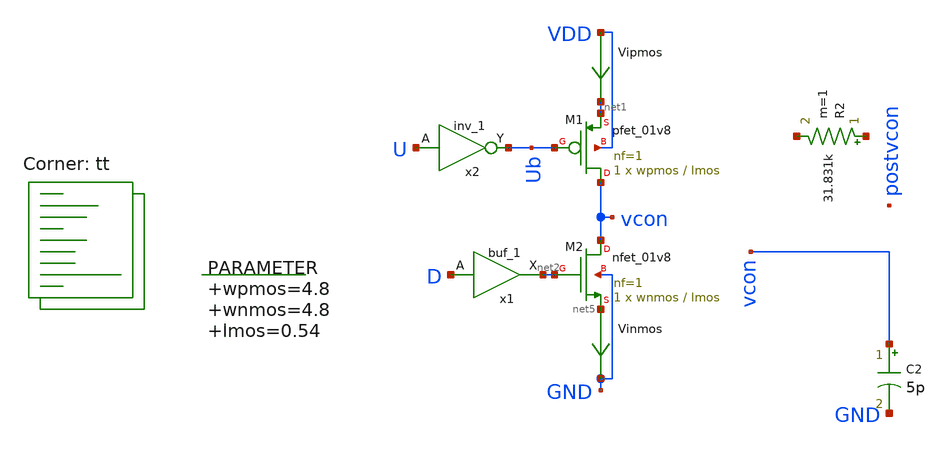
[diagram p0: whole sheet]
** sch_path: xschem/charge_pump-tb.sch
**.subckt charge_pump-tb
.param wpmos=4.8 wnmos=4.8 lmos=0.54
C2 vcon GND 5p m=1
R2 net3 net4 31.831k m=1
XM1 vcon Ub net1 VDD sky130_fd_pr__pfet_01v8 L=lmos W=wpmos nf=1 ad='int((nf+1)/2) * W/nf * 0.29' as='int((nf+2)/2) * W/nf * 0.29'
+ pd='2*int((nf+1)/2) * (W/nf + 0.29)' ps='2*int((nf+2)/2) * (W/nf + 0.29)' nrd='0.29 / W' nrs='0.29 / W'
+ sa=0 sb=0 sd=0 mult=1 m=1
XM2 vcon net2 net5 GND sky130_fd_pr__nfet_01v8 L=lmos W=wnmos nf=1 ad='int((nf+1)/2) * W/nf * 0.29' as='int((nf+2)/2) * W/nf * 0.29'
+ pd='2*int((nf+1)/2) * (W/nf + 0.29)' ps='2*int((nf+2)/2) * (W/nf + 0.29)' nrd='0.29 / W' nrs='0.29 / W'
+ sa=0 sb=0 sd=0 mult=1 m=1
x2 U GND GND VDD VDD Ub sky130_fd_sc_hd__inv_1
Vipmos VDD net1 0
.save i(vipmos)
Vinmos net5 GND 0
.save i(vinmos)
x1 D GND GND VDD VDD net2 sky130_fd_sc_hd__buf_1
**** begin user architecture code
 .lib $::SKYWATER_MODELS/sky130.lib.spice tt
.include $::SKYWATER_STDCELLS/sky130_fd_sc_hd.spice
.param mc_mm_switch = 0
.param mc_pr_switch = 0




  .param max_freq=100e6 period={1/max_freq} time_high={period/2}
  .param delay_vin1={time_high} delay_vin2={time_high*2}

  .option wnflag=1
  .option safecurrents

  Vvdd  VDD GND dc 1.8
  Vin1 U GND pulse(0 1.8 {delay_vin1} 1p 1p {time_high/3} {period})
  Vin2 D GND pulse(0 1.8 {delay_vin2} 1p 1p {time_high/3} {period})

  .control
     reset
     save all
     tran 0.01n 500n
     write charge_pump-tb.raw
     set appendwrite

     alterparam lmos=0.36
     reset
     save all
     tran 0.01n 500n
     write charge_pump-tb.raw

     *set appendwrite

     *1=0 1.5=90 2=180 3=360
     *let phase=1

     *while phase <= 2
      *alter @vin2[PULSE] [ 0 1.8 {delay_vin2*$&phase} 1p 1p {time_high} {period}) ]
      *reset
      *save all
      *tran 0.01n 300n
      *write pll-tb.raw
      *let phase = phase + 0.25
     *end
    quit 0
  .endc



**** end user architecture code
**.ends
.end
